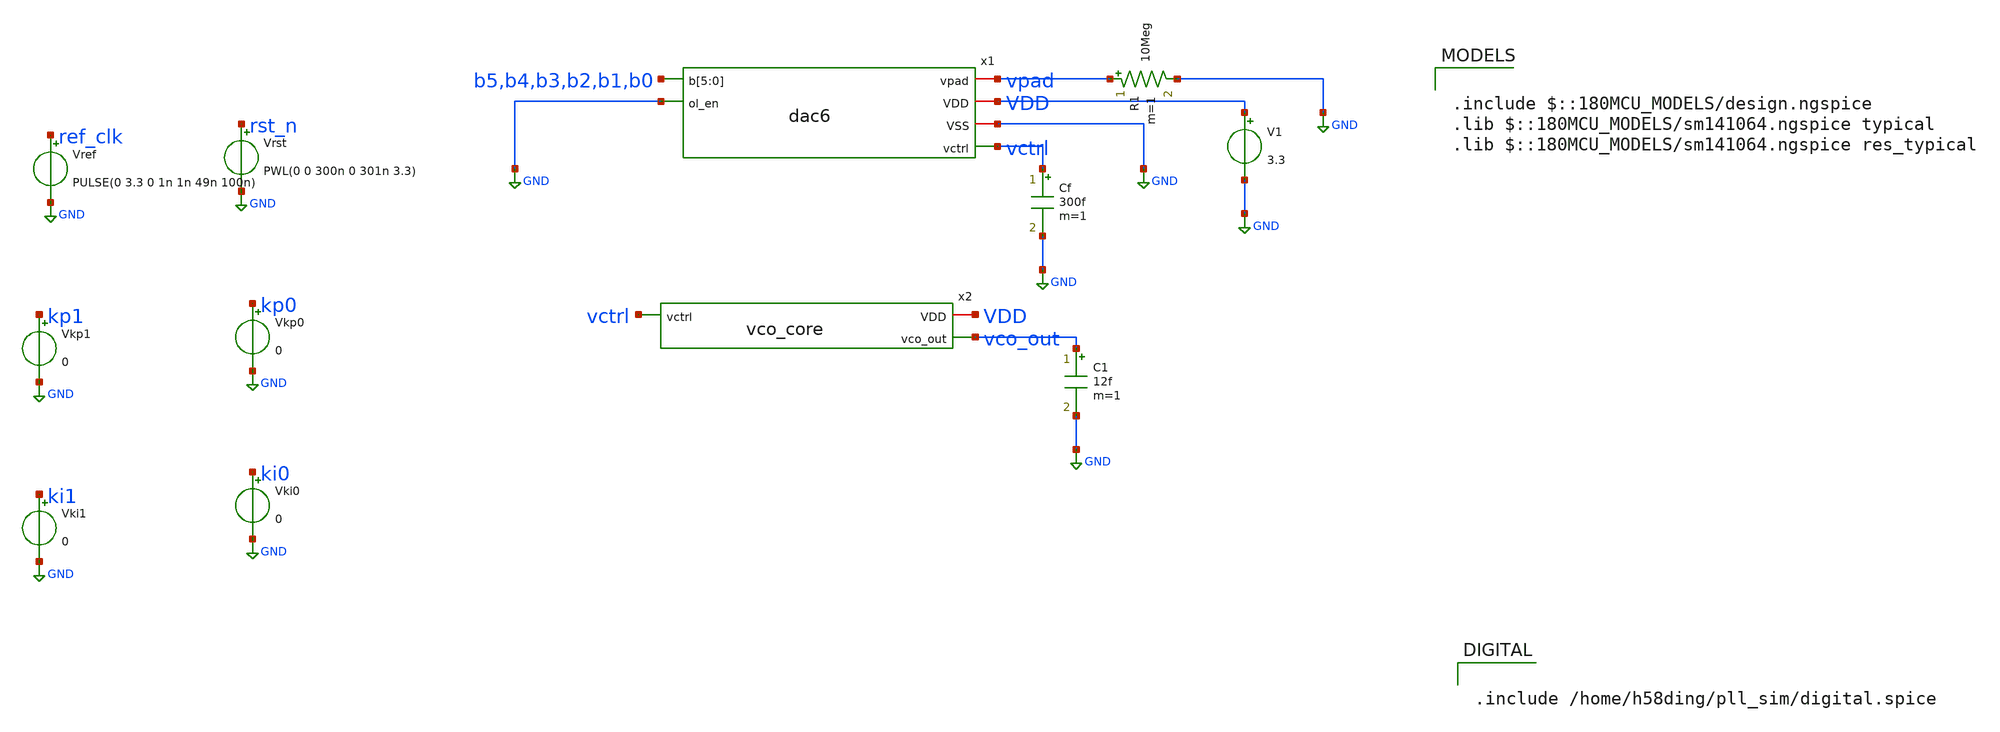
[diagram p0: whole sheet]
** sch_path: analog/tb_pll.sch
**.subckt tb_pll
x1 b5 b4 b3 b2 b1 b0 GND vpad VDD GND vctrl dac6
V1 VDD GND 3.3
R1 vpad GND 10Meg m=1
Vrst rst_n GND PWL(0 0 300n 0 301n 3.3)
Vref ref_clk GND PULSE(0 3.3 0 1n 1n 49n 100n)
Vkp0 kp0 GND 0
Vkp1 kp1 GND 0
Vki0 ki0 GND 0
Vki1 ki1 GND 0
x2 VDD vctrl vco_out vco_core
C1 vco_out GND 12f m=1
Cf vctrl GND 300f m=1
**** begin user architecture code

.include $::180MCU_MODELS/design.ngspice
.lib $::180MCU_MODELS/sm141064.ngspice typical
.lib $::180MCU_MODELS/sm141064.ngspice res_typical



.ic v(x2.n0)=0 v(x2.n1)=3.3 v(x2.n2)=0 v(x2.n3)=3.3 v(x2.n4)=0
.control
save v(vco_out) v(vctrl)
tran 0.1n 40u 10u
plot v(vctrl)
linearize v(vco_out)
set specwindow=hanning
fft v(vco_out)
let mag = db(mag(v(vco_out)))
meas sp f_peak max_at mag from=60e6 to=100e6
meas sp peak max mag from=60e6 to=100e6
meas sp spur_low max mag from=75e6 to=79e6
meas sp spur_high max mag from=81e6 to=85e6
let dbc_low = spur_low - peak
let dbc_high = spur_high - peak
print dbc_low dbc_high
plot mag xlimit 70e6 90e6 title VCO_spectrum
.endc




.include /home/h58ding/pll_sim/digital.spice


**** end user architecture code
**.ends

* expanding   symbol:  pll_dac/dac6.sym # of pins=6
** sym_path: xschem/pll_dac/dac6.sym
** sch_path: xschem/pll_dac/dac6.sch
.subckt dac6 b[5] b[4] b[3] b[2] b[1] b[0] ol_en vpad VDD VSS vctrl
*.ipin b[5],b[4],b[3],b[2],b[1],b[0]
*.ipin ol_en
*.iopin vpad
*.iopin VDD
*.iopin VSS
*.opin vctrl
x1 VDD b[5] b[4] b[3] b[2] b[1] b[0] VSS vctrl schr2r6
XRD1 rd vctrl VSS ppolyf_u_1k r_width=1u r_length=61u m=1
XRD2[1] VSS rd VSS ppolyf_u_1k r_width=1u r_length=61u m=1
XRD2[0] VSS rd VSS ppolyf_u_1k r_width=1u r_length=61u m=1
XOL VDD ol_en ol_en_b VSS sw_inv
XM2 vctrl ol_en_b vpad VDD pfet_03v3 L=0.28u W=5.6u nf=1 ad='int((nf+1)/2) * W/nf * 0.18u' as='int((nf+2)/2) * W/nf * 0.18u'
+ pd='2*int((nf+1)/2) * (W/nf + 0.18u)' ps='2*int((nf+2)/2) * (W/nf + 0.18u)' nrd='0.18u / W' nrs='0.18u / W'
+ sa=0 sb=0 sd=0 m=1
XM1 vctrl ol_en vpad VSS nfet_03v3 L=0.28u W=2u nf=1 ad='int((nf+1)/2) * W/nf * 0.18u' as='int((nf+2)/2) * W/nf * 0.18u'
+ pd='2*int((nf+1)/2) * (W/nf + 0.18u)' ps='2*int((nf+2)/2) * (W/nf + 0.18u)' nrd='0.18u / W' nrs='0.18u / W'
+ sa=0 sb=0 sd=0 m=1
.ends


* expanding   symbol:  GF180-PLL/analog/vco/vco_core.sym # of pins=3
** sym_path: analog/vco/vco_core.sym
** sch_path: analog/vco/vco_core.sch
.subckt vco_core VDD vctrl vco_out
*.iopin VDD
*.ipin vctrl
*.opin vco_out
XM1 Vbiasn vctrl net1 net1 pfet_03v3 L=1u W=8u nf=1 ad='int((nf+1)/2) * W/nf * 0.18u' as='int((nf+2)/2) * W/nf * 0.18u'
+ pd='2*int((nf+1)/2) * (W/nf + 0.18u)' ps='2*int((nf+2)/2) * (W/nf + 0.18u)' nrd='0.18u / W' nrs='0.18u / W'
+ sa=0 sb=0 sd=0 m=1
XM2 Vbiasn Vbiasn GND GND nfet_03v3 L=1u W=3u nf=1 ad='int((nf+1)/2) * W/nf * 0.18u' as='int((nf+2)/2) * W/nf * 0.18u'
+ pd='2*int((nf+1)/2) * (W/nf + 0.18u)' ps='2*int((nf+2)/2) * (W/nf + 0.18u)' nrd='0.18u / W' nrs='0.18u / W'
+ sa=0 sb=0 sd=0 m=1
XM3 Vbiasp Vbiasn GND GND nfet_03v3 L=1u W=3u nf=1 ad='int((nf+1)/2) * W/nf * 0.18u' as='int((nf+2)/2) * W/nf * 0.18u'
+ pd='2*int((nf+1)/2) * (W/nf + 0.18u)' ps='2*int((nf+2)/2) * (W/nf + 0.18u)' nrd='0.18u / W' nrs='0.18u / W'
+ sa=0 sb=0 sd=0 m=1
XM4 Vbiasp Vbiasp VDD VDD pfet_03v3 L=1u W=3u nf=1 ad='int((nf+1)/2) * W/nf * 0.18u' as='int((nf+2)/2) * W/nf * 0.18u'
+ pd='2*int((nf+1)/2) * (W/nf + 0.18u)' ps='2*int((nf+2)/2) * (W/nf + 0.18u)' nrd='0.18u / W' nrs='0.18u / W'
+ sa=0 sb=0 sd=0 m=1
XR1 net1 VDD GND ppolyf_u r_width=1u r_length=189u m=1
XM5 net2 Vbiasn GND GND nfet_03v3 L=1u W=3u nf=1 ad='int((nf+1)/2) * W/nf * 0.18u' as='int((nf+2)/2) * W/nf * 0.18u'
+ pd='2*int((nf+1)/2) * (W/nf + 0.18u)' ps='2*int((nf+2)/2) * (W/nf + 0.18u)' nrd='0.18u / W' nrs='0.18u / W'
+ sa=0 sb=0 sd=0 m=1
XM6 n0 n4 net2 GND nfet_03v3 L=0.28u W=1u nf=1 ad='int((nf+1)/2) * W/nf * 0.18u' as='int((nf+2)/2) * W/nf * 0.18u'
+ pd='2*int((nf+1)/2) * (W/nf + 0.18u)' ps='2*int((nf+2)/2) * (W/nf + 0.18u)' nrd='0.18u / W' nrs='0.18u / W'
+ sa=0 sb=0 sd=0 m=1
XM7 n0 n4 net3 VDD pfet_03v3 L=0.28u W=2u nf=1 ad='int((nf+1)/2) * W/nf * 0.18u' as='int((nf+2)/2) * W/nf * 0.18u'
+ pd='2*int((nf+1)/2) * (W/nf + 0.18u)' ps='2*int((nf+2)/2) * (W/nf + 0.18u)' nrd='0.18u / W' nrs='0.18u / W'
+ sa=0 sb=0 sd=0 m=1
XM8 net3 Vbiasp VDD VDD pfet_03v3 L=1u W=3u nf=1 ad='int((nf+1)/2) * W/nf * 0.18u' as='int((nf+2)/2) * W/nf * 0.18u'
+ pd='2*int((nf+1)/2) * (W/nf + 0.18u)' ps='2*int((nf+2)/2) * (W/nf + 0.18u)' nrd='0.18u / W' nrs='0.18u / W'
+ sa=0 sb=0 sd=0 m=1
XM9 net4 Vbiasn GND GND nfet_03v3 L=1u W=3u nf=1 ad='int((nf+1)/2) * W/nf * 0.18u' as='int((nf+2)/2) * W/nf * 0.18u'
+ pd='2*int((nf+1)/2) * (W/nf + 0.18u)' ps='2*int((nf+2)/2) * (W/nf + 0.18u)' nrd='0.18u / W' nrs='0.18u / W'
+ sa=0 sb=0 sd=0 m=1
XM10 n1 n0 net4 GND nfet_03v3 L=0.28u W=1u nf=1 ad='int((nf+1)/2) * W/nf * 0.18u' as='int((nf+2)/2) * W/nf * 0.18u'
+ pd='2*int((nf+1)/2) * (W/nf + 0.18u)' ps='2*int((nf+2)/2) * (W/nf + 0.18u)' nrd='0.18u / W' nrs='0.18u / W'
+ sa=0 sb=0 sd=0 m=1
XM11 n1 n0 net5 VDD pfet_03v3 L=0.28u W=2u nf=1 ad='int((nf+1)/2) * W/nf * 0.18u' as='int((nf+2)/2) * W/nf * 0.18u'
+ pd='2*int((nf+1)/2) * (W/nf + 0.18u)' ps='2*int((nf+2)/2) * (W/nf + 0.18u)' nrd='0.18u / W' nrs='0.18u / W'
+ sa=0 sb=0 sd=0 m=1
XM12 net5 Vbiasp VDD VDD pfet_03v3 L=1u W=3u nf=1 ad='int((nf+1)/2) * W/nf * 0.18u' as='int((nf+2)/2) * W/nf * 0.18u'
+ pd='2*int((nf+1)/2) * (W/nf + 0.18u)' ps='2*int((nf+2)/2) * (W/nf + 0.18u)' nrd='0.18u / W' nrs='0.18u / W'
+ sa=0 sb=0 sd=0 m=1
XM13 net6 Vbiasn GND GND nfet_03v3 L=1u W=3u nf=1 ad='int((nf+1)/2) * W/nf * 0.18u' as='int((nf+2)/2) * W/nf * 0.18u'
+ pd='2*int((nf+1)/2) * (W/nf + 0.18u)' ps='2*int((nf+2)/2) * (W/nf + 0.18u)' nrd='0.18u / W' nrs='0.18u / W'
+ sa=0 sb=0 sd=0 m=1
XM14 n2 n1 net6 GND nfet_03v3 L=0.28u W=1u nf=1 ad='int((nf+1)/2) * W/nf * 0.18u' as='int((nf+2)/2) * W/nf * 0.18u'
+ pd='2*int((nf+1)/2) * (W/nf + 0.18u)' ps='2*int((nf+2)/2) * (W/nf + 0.18u)' nrd='0.18u / W' nrs='0.18u / W'
+ sa=0 sb=0 sd=0 m=1
XM15 n2 n1 net7 VDD pfet_03v3 L=0.28u W=2u nf=1 ad='int((nf+1)/2) * W/nf * 0.18u' as='int((nf+2)/2) * W/nf * 0.18u'
+ pd='2*int((nf+1)/2) * (W/nf + 0.18u)' ps='2*int((nf+2)/2) * (W/nf + 0.18u)' nrd='0.18u / W' nrs='0.18u / W'
+ sa=0 sb=0 sd=0 m=1
XM16 net7 Vbiasp VDD VDD pfet_03v3 L=1u W=3u nf=1 ad='int((nf+1)/2) * W/nf * 0.18u' as='int((nf+2)/2) * W/nf * 0.18u'
+ pd='2*int((nf+1)/2) * (W/nf + 0.18u)' ps='2*int((nf+2)/2) * (W/nf + 0.18u)' nrd='0.18u / W' nrs='0.18u / W'
+ sa=0 sb=0 sd=0 m=1
XM17 net8 Vbiasn GND GND nfet_03v3 L=1u W=3u nf=1 ad='int((nf+1)/2) * W/nf * 0.18u' as='int((nf+2)/2) * W/nf * 0.18u'
+ pd='2*int((nf+1)/2) * (W/nf + 0.18u)' ps='2*int((nf+2)/2) * (W/nf + 0.18u)' nrd='0.18u / W' nrs='0.18u / W'
+ sa=0 sb=0 sd=0 m=1
XM18 n3 n2 net8 GND nfet_03v3 L=0.28u W=1u nf=1 ad='int((nf+1)/2) * W/nf * 0.18u' as='int((nf+2)/2) * W/nf * 0.18u'
+ pd='2*int((nf+1)/2) * (W/nf + 0.18u)' ps='2*int((nf+2)/2) * (W/nf + 0.18u)' nrd='0.18u / W' nrs='0.18u / W'
+ sa=0 sb=0 sd=0 m=1
XM19 n3 n2 net9 VDD pfet_03v3 L=0.28u W=2u nf=1 ad='int((nf+1)/2) * W/nf * 0.18u' as='int((nf+2)/2) * W/nf * 0.18u'
+ pd='2*int((nf+1)/2) * (W/nf + 0.18u)' ps='2*int((nf+2)/2) * (W/nf + 0.18u)' nrd='0.18u / W' nrs='0.18u / W'
+ sa=0 sb=0 sd=0 m=1
XM20 net9 Vbiasp VDD VDD pfet_03v3 L=1u W=3u nf=1 ad='int((nf+1)/2) * W/nf * 0.18u' as='int((nf+2)/2) * W/nf * 0.18u'
+ pd='2*int((nf+1)/2) * (W/nf + 0.18u)' ps='2*int((nf+2)/2) * (W/nf + 0.18u)' nrd='0.18u / W' nrs='0.18u / W'
+ sa=0 sb=0 sd=0 m=1
XM21 net10 Vbiasn GND GND nfet_03v3 L=1u W=3u nf=1 ad='int((nf+1)/2) * W/nf * 0.18u' as='int((nf+2)/2) * W/nf * 0.18u'
+ pd='2*int((nf+1)/2) * (W/nf + 0.18u)' ps='2*int((nf+2)/2) * (W/nf + 0.18u)' nrd='0.18u / W' nrs='0.18u / W'
+ sa=0 sb=0 sd=0 m=1
XM22 n4 n3 net10 GND nfet_03v3 L=0.28u W=1u nf=1 ad='int((nf+1)/2) * W/nf * 0.18u' as='int((nf+2)/2) * W/nf * 0.18u'
+ pd='2*int((nf+1)/2) * (W/nf + 0.18u)' ps='2*int((nf+2)/2) * (W/nf + 0.18u)' nrd='0.18u / W' nrs='0.18u / W'
+ sa=0 sb=0 sd=0 m=1
XM23 n4 n3 net11 VDD pfet_03v3 L=0.28u W=2u nf=1 ad='int((nf+1)/2) * W/nf * 0.18u' as='int((nf+2)/2) * W/nf * 0.18u'
+ pd='2*int((nf+1)/2) * (W/nf + 0.18u)' ps='2*int((nf+2)/2) * (W/nf + 0.18u)' nrd='0.18u / W' nrs='0.18u / W'
+ sa=0 sb=0 sd=0 m=1
XM24 net11 Vbiasp VDD VDD pfet_03v3 L=1u W=3u nf=1 ad='int((nf+1)/2) * W/nf * 0.18u' as='int((nf+2)/2) * W/nf * 0.18u'
+ pd='2*int((nf+1)/2) * (W/nf + 0.18u)' ps='2*int((nf+2)/2) * (W/nf + 0.18u)' nrd='0.18u / W' nrs='0.18u / W'
+ sa=0 sb=0 sd=0 m=1
C1 n0 GND 3f m=1
C2 n1 GND 3f m=1
C3 n2 GND 3f m=1
C4 n3 GND 3f m=1
C5 n4 GND 3f m=1
XM25 net12 n4 GND GND nfet_03v3 L=0.28u W=1u nf=1 ad='int((nf+1)/2) * W/nf * 0.18u' as='int((nf+2)/2) * W/nf * 0.18u'
+ pd='2*int((nf+1)/2) * (W/nf + 0.18u)' ps='2*int((nf+2)/2) * (W/nf + 0.18u)' nrd='0.18u / W' nrs='0.18u / W'
+ sa=0 sb=0 sd=0 m=1
XM26 net12 n4 VDD VDD pfet_03v3 L=0.28u W=2u nf=1 ad='int((nf+1)/2) * W/nf * 0.18u' as='int((nf+2)/2) * W/nf * 0.18u'
+ pd='2*int((nf+1)/2) * (W/nf + 0.18u)' ps='2*int((nf+2)/2) * (W/nf + 0.18u)' nrd='0.18u / W' nrs='0.18u / W'
+ sa=0 sb=0 sd=0 m=1
XM27 vco_out net12 GND GND nfet_03v3 L=0.28u W=1u nf=1 ad='int((nf+1)/2) * W/nf * 0.18u' as='int((nf+2)/2) * W/nf * 0.18u'
+ pd='2*int((nf+1)/2) * (W/nf + 0.18u)' ps='2*int((nf+2)/2) * (W/nf + 0.18u)' nrd='0.18u / W' nrs='0.18u / W'
+ sa=0 sb=0 sd=0 m=1
XM28 vco_out net12 VDD VDD pfet_03v3 L=0.28u W=2u nf=1 ad='int((nf+1)/2) * W/nf * 0.18u' as='int((nf+2)/2) * W/nf * 0.18u'
+ pd='2*int((nf+1)/2) * (W/nf + 0.18u)' ps='2*int((nf+2)/2) * (W/nf + 0.18u)' nrd='0.18u / W' nrs='0.18u / W'
+ sa=0 sb=0 sd=0 m=1
C7 net12 GND 3f m=1
.ends


* expanding   symbol:  pll_dac/schr2r6.sym # of pins=4
** sym_path: xschem/pll_dac/schr2r6.sym
** sch_path: xschem/pll_dac/schr2r6.sch
.subckt schr2r6 VDD b[5] b[4] b[3] b[2] b[1] b[0] VSS lad
*.iopin VDD
*.iopin VSS
*.ipin b[5],b[4],b[3],b[2],b[1],b[0]
*.opin lad
XI[5] VDD b[5] d[5] VSS sw_inv
XI[4] VDD b[4] d[4] VSS sw_inv
XI[3] VDD b[3] d[3] VSS sw_inv
XI[2] VDD b[2] d[2] VSS sw_inv
XI[1] VDD b[1] d[1] VSS sw_inv
XI[0] VDD b[0] d[0] VSS sw_inv
XIT VDD VDD dt VSS sw_inv
XRLa[5] m[5] d[5] VSS ppolyf_u_1k r_width=1u r_length=61u m=1
XRLa[4] m[4] d[4] VSS ppolyf_u_1k r_width=1u r_length=61u m=1
XRLa[3] m[3] d[3] VSS ppolyf_u_1k r_width=1u r_length=61u m=1
XRLa[2] m[2] d[2] VSS ppolyf_u_1k r_width=1u r_length=61u m=1
XRLa[1] m[1] d[1] VSS ppolyf_u_1k r_width=1u r_length=61u m=1
XRLa[0] m[0] d[0] VSS ppolyf_u_1k r_width=1u r_length=61u m=1
XRLb[5] lad m[5] VSS ppolyf_u_1k r_width=1u r_length=61u m=1
XRLb[4] j[4] m[4] VSS ppolyf_u_1k r_width=1u r_length=61u m=1
XRLb[3] j[3] m[3] VSS ppolyf_u_1k r_width=1u r_length=61u m=1
XRLb[2] j[2] m[2] VSS ppolyf_u_1k r_width=1u r_length=61u m=1
XRLb[1] j[1] m[1] VSS ppolyf_u_1k r_width=1u r_length=61u m=1
XRLb[0] j[0] m[0] VSS ppolyf_u_1k r_width=1u r_length=61u m=1
XRR[4] lad j[4] VSS ppolyf_u_1k r_width=1u r_length=61u m=1
XRR[3] j[4] j[3] VSS ppolyf_u_1k r_width=1u r_length=61u m=1
XRR[2] j[3] j[2] VSS ppolyf_u_1k r_width=1u r_length=61u m=1
XRR[1] j[2] j[1] VSS ppolyf_u_1k r_width=1u r_length=61u m=1
XRR[0] j[1] j[0] VSS ppolyf_u_1k r_width=1u r_length=61u m=1
XRTa mt dt VSS ppolyf_u_1k r_width=1u r_length=61u m=1
XRTb j[0] mt VSS ppolyf_u_1k r_width=1u r_length=61u m=1
XRDUM[3] VSS VSS VSS ppolyf_u_1k r_width=1u r_length=61u m=1
XRDUM[2] VSS VSS VSS ppolyf_u_1k r_width=1u r_length=61u m=1
XRDUM[1] VSS VSS VSS ppolyf_u_1k r_width=1u r_length=61u m=1
XRDUM[0] VSS VSS VSS ppolyf_u_1k r_width=1u r_length=61u m=1
.ends


* expanding   symbol:  pll_dac/sw_inv.sym # of pins=4
** sym_path: xschem/pll_dac/sw_inv.sym
** sch_path: xschem/pll_dac/sw_inv.sch
.subckt sw_inv VDD A Y VSS
*.ipin A
*.iopin VDD
*.iopin VSS
*.opin Y
XM1 Y A VSS VSS nfet_03v3 L=0.28u W=2u nf=1 ad='int((nf+1)/2) * W/nf * 0.18u' as='int((nf+2)/2) * W/nf * 0.18u'
+ pd='2*int((nf+1)/2) * (W/nf + 0.18u)' ps='2*int((nf+2)/2) * (W/nf + 0.18u)' nrd='0.18u / W' nrs='0.18u / W'
+ sa=0 sb=0 sd=0 m=1
XM2 Y A VDD VDD pfet_03v3 L=0.28u W=5.6u nf=1 ad='int((nf+1)/2) * W/nf * 0.18u' as='int((nf+2)/2) * W/nf * 0.18u'
+ pd='2*int((nf+1)/2) * (W/nf + 0.18u)' ps='2*int((nf+2)/2) * (W/nf + 0.18u)' nrd='0.18u / W' nrs='0.18u / W'
+ sa=0 sb=0 sd=0 m=1
.ends

.GLOBAL GND
.end
